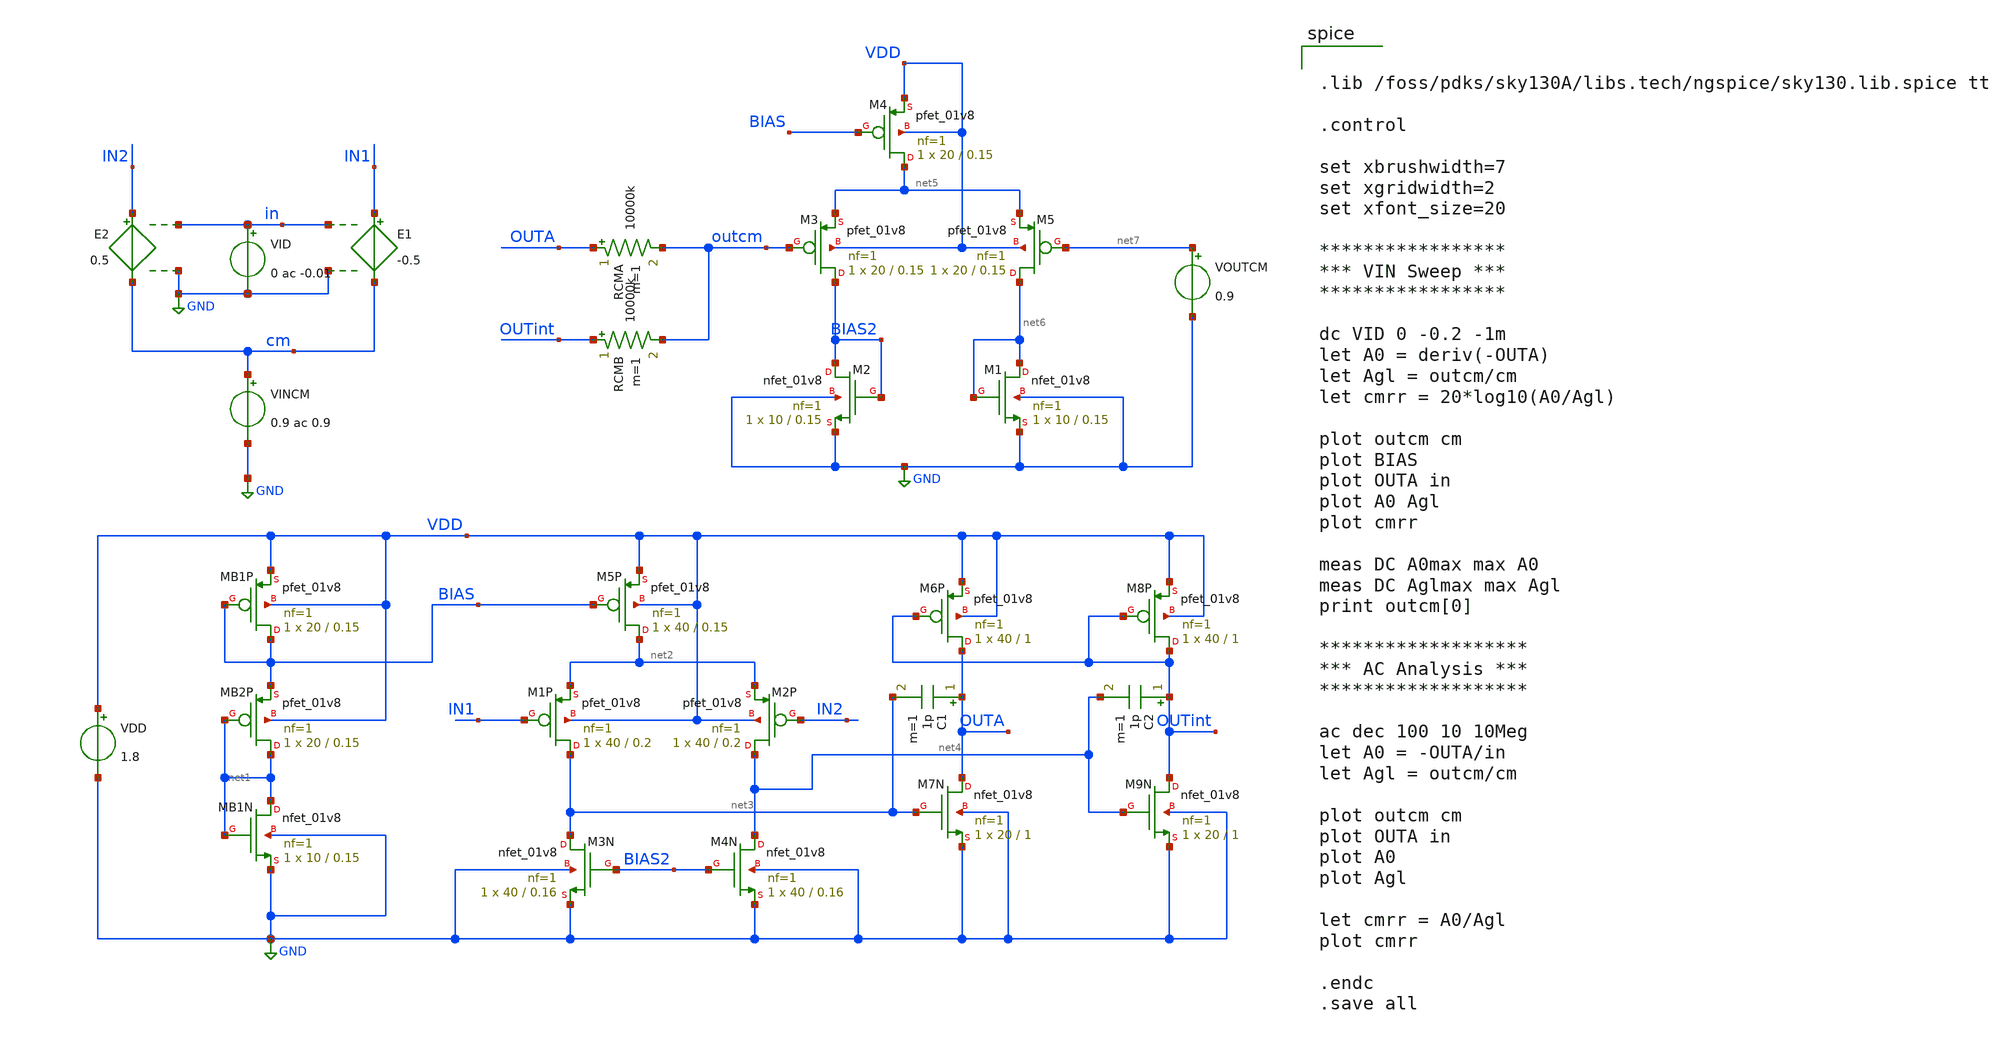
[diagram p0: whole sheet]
** sch_path: designs/Aufgabe2_k12136610.sch
**.subckt Aufgabe2_k12136610
VINCM cm GND 0.9 ac 0.9
XMB1N net1 net1 GND GND sky130_fd_pr__nfet_01v8 L=0.15 W=10 nf=1 ad='int((nf+1)/2) * W/nf * 0.29' as='int((nf+2)/2) * W/nf * 0.29'
+ pd='2*int((nf+1)/2) * (W/nf + 0.29)' ps='2*int((nf+2)/2) * (W/nf + 0.29)' nrd='0.29 / W' nrs='0.29 / W'
+ sa=0 sb=0 sd=0 mult=1 m=1
XMB2P net1 net1 BIAS VDD sky130_fd_pr__pfet_01v8 L=0.15 W=20 nf=1 ad='int((nf+1)/2) * W/nf * 0.29' as='int((nf+2)/2) * W/nf * 0.29'
+ pd='2*int((nf+1)/2) * (W/nf + 0.29)' ps='2*int((nf+2)/2) * (W/nf + 0.29)' nrd='0.29 / W' nrs='0.29 / W'
+ sa=0 sb=0 sd=0 mult=1 m=1
XMB1P BIAS BIAS VDD VDD sky130_fd_pr__pfet_01v8 L=0.15 W=20 nf=1 ad='int((nf+1)/2) * W/nf * 0.29' as='int((nf+2)/2) * W/nf * 0.29'
+ pd='2*int((nf+1)/2) * (W/nf + 0.29)' ps='2*int((nf+2)/2) * (W/nf + 0.29)' nrd='0.29 / W' nrs='0.29 / W'
+ sa=0 sb=0 sd=0 mult=1 m=1
XM5P net2 BIAS VDD VDD sky130_fd_pr__pfet_01v8 L=0.15 W=40 nf=1 ad='int((nf+1)/2) * W/nf * 0.29' as='int((nf+2)/2) * W/nf * 0.29'
+ pd='2*int((nf+1)/2) * (W/nf + 0.29)' ps='2*int((nf+2)/2) * (W/nf + 0.29)' nrd='0.29 / W' nrs='0.29 / W'
+ sa=0 sb=0 sd=0 mult=1 m=1
XM1P net3 IN1 net2 VDD sky130_fd_pr__pfet_01v8 L=0.2 W=40 nf=1 ad='int((nf+1)/2) * W/nf * 0.29' as='int((nf+2)/2) * W/nf * 0.29'
+ pd='2*int((nf+1)/2) * (W/nf + 0.29)' ps='2*int((nf+2)/2) * (W/nf + 0.29)' nrd='0.29 / W' nrs='0.29 / W'
+ sa=0 sb=0 sd=0 mult=1 m=1
XM2P net4 IN2 net2 VDD sky130_fd_pr__pfet_01v8 L=0.2 W=40 nf=1 ad='int((nf+1)/2) * W/nf * 0.29' as='int((nf+2)/2) * W/nf * 0.29'
+ pd='2*int((nf+1)/2) * (W/nf + 0.29)' ps='2*int((nf+2)/2) * (W/nf + 0.29)' nrd='0.29 / W' nrs='0.29 / W'
+ sa=0 sb=0 sd=0 mult=1 m=1
XM4N net4 BIAS2 GND GND sky130_fd_pr__nfet_01v8 L=0.16 W=40 nf=1 ad='int((nf+1)/2) * W/nf * 0.29' as='int((nf+2)/2) * W/nf * 0.29'
+ pd='2*int((nf+1)/2) * (W/nf + 0.29)' ps='2*int((nf+2)/2) * (W/nf + 0.29)' nrd='0.29 / W' nrs='0.29 / W'
+ sa=0 sb=0 sd=0 mult=1 m=1
XM3N net3 BIAS2 GND GND sky130_fd_pr__nfet_01v8 L=0.16 W=40 nf=1 ad='int((nf+1)/2) * W/nf * 0.29' as='int((nf+2)/2) * W/nf * 0.29'
+ pd='2*int((nf+1)/2) * (W/nf + 0.29)' ps='2*int((nf+2)/2) * (W/nf + 0.29)' nrd='0.29 / W' nrs='0.29 / W'
+ sa=0 sb=0 sd=0 mult=1 m=1
XM6P OUTA OUTint VDD VDD sky130_fd_pr__pfet_01v8 L=1 W=40 nf=1 ad='int((nf+1)/2) * W/nf * 0.29' as='int((nf+2)/2) * W/nf * 0.29'
+ pd='2*int((nf+1)/2) * (W/nf + 0.29)' ps='2*int((nf+2)/2) * (W/nf + 0.29)' nrd='0.29 / W' nrs='0.29 / W'
+ sa=0 sb=0 sd=0 mult=1 m=1
XM8P OUTint OUTint VDD VDD sky130_fd_pr__pfet_01v8 L=1 W=40 nf=1 ad='int((nf+1)/2) * W/nf * 0.29' as='int((nf+2)/2) * W/nf * 0.29'
+ pd='2*int((nf+1)/2) * (W/nf + 0.29)' ps='2*int((nf+2)/2) * (W/nf + 0.29)' nrd='0.29 / W' nrs='0.29 / W'
+ sa=0 sb=0 sd=0 mult=1 m=1
XM7N OUTA net3 GND GND sky130_fd_pr__nfet_01v8 L=1 W=20 nf=1 ad='int((nf+1)/2) * W/nf * 0.29' as='int((nf+2)/2) * W/nf * 0.29'
+ pd='2*int((nf+1)/2) * (W/nf + 0.29)' ps='2*int((nf+2)/2) * (W/nf + 0.29)' nrd='0.29 / W' nrs='0.29 / W'
+ sa=0 sb=0 sd=0 mult=1 m=1
XM9N OUTint net4 GND GND sky130_fd_pr__nfet_01v8 L=1 W=20 nf=1 ad='int((nf+1)/2) * W/nf * 0.29' as='int((nf+2)/2) * W/nf * 0.29'
+ pd='2*int((nf+1)/2) * (W/nf + 0.29)' ps='2*int((nf+2)/2) * (W/nf + 0.29)' nrd='0.29 / W' nrs='0.29 / W'
+ sa=0 sb=0 sd=0 mult=1 m=1
C1 OUTA net3 1p m=1
C2 OUTint net4 1p m=1
VDD VDD GND 1.8
XM4 net5 BIAS VDD VDD sky130_fd_pr__pfet_01v8 L=0.15 W=20 nf=1 ad='int((nf+1)/2) * W/nf * 0.29' as='int((nf+2)/2) * W/nf * 0.29'
+ pd='2*int((nf+1)/2) * (W/nf + 0.29)' ps='2*int((nf+2)/2) * (W/nf + 0.29)' nrd='0.29 / W' nrs='0.29 / W'
+ sa=0 sb=0 sd=0 mult=1 m=1
XM3 BIAS2 outcm net5 VDD sky130_fd_pr__pfet_01v8 L=0.15 W=20 nf=1 ad='int((nf+1)/2) * W/nf * 0.29' as='int((nf+2)/2) * W/nf * 0.29'
+ pd='2*int((nf+1)/2) * (W/nf + 0.29)' ps='2*int((nf+2)/2) * (W/nf + 0.29)' nrd='0.29 / W' nrs='0.29 / W'
+ sa=0 sb=0 sd=0 mult=1 m=1
XM5 net6 net7 net5 VDD sky130_fd_pr__pfet_01v8 L=0.15 W=20 nf=1 ad='int((nf+1)/2) * W/nf * 0.29' as='int((nf+2)/2) * W/nf * 0.29'
+ pd='2*int((nf+1)/2) * (W/nf + 0.29)' ps='2*int((nf+2)/2) * (W/nf + 0.29)' nrd='0.29 / W' nrs='0.29 / W'
+ sa=0 sb=0 sd=0 mult=1 m=1
XM1 net6 net6 GND GND sky130_fd_pr__nfet_01v8 L=0.15 W=10 nf=1 ad='int((nf+1)/2) * W/nf * 0.29' as='int((nf+2)/2) * W/nf * 0.29'
+ pd='2*int((nf+1)/2) * (W/nf + 0.29)' ps='2*int((nf+2)/2) * (W/nf + 0.29)' nrd='0.29 / W' nrs='0.29 / W'
+ sa=0 sb=0 sd=0 mult=1 m=1
XM2 BIAS2 BIAS2 GND GND sky130_fd_pr__nfet_01v8 L=0.15 W=10 nf=1 ad='int((nf+1)/2) * W/nf * 0.29' as='int((nf+2)/2) * W/nf * 0.29'
+ pd='2*int((nf+1)/2) * (W/nf + 0.29)' ps='2*int((nf+2)/2) * (W/nf + 0.29)' nrd='0.29 / W' nrs='0.29 / W'
+ sa=0 sb=0 sd=0 mult=1 m=1
RCMA OUTA outcm 10000k m=1
RCMB OUTint outcm 10000k m=1
VOUTCM net7 GND 0.9
VID in GND 0 ac -0.01
E1 IN1 cm in GND -0.5
E2 IN2 cm in GND 0.5
**** begin user architecture code


.lib /foss/pdks/sky130A/libs.tech/ngspice/sky130.lib.spice tt

.control

set xbrushwidth=7
set xgridwidth=2
set xfont_size=20

*****************
*** VIN Sweep ***
*****************

dc VID 0 -0.2 -1m
let A0 = deriv(-OUTA)
let Agl = outcm/cm
let cmrr = 20*log10(A0/Agl)

plot outcm cm
plot BIAS
plot OUTA in
plot A0 Agl
plot cmrr

meas DC A0max max A0
meas DC Aglmax max Agl
print outcm[0]

*******************
*** AC Analysis ***
*******************

ac dec 100 10 10Meg
let A0 = -OUTA/in
let Agl = outcm/cm

plot outcm cm
plot OUTA in
plot A0
plot Agl

let cmrr = A0/Agl
plot cmrr

.endc
.save all


**** end user architecture code
**.ends
.GLOBAL GND
.end
